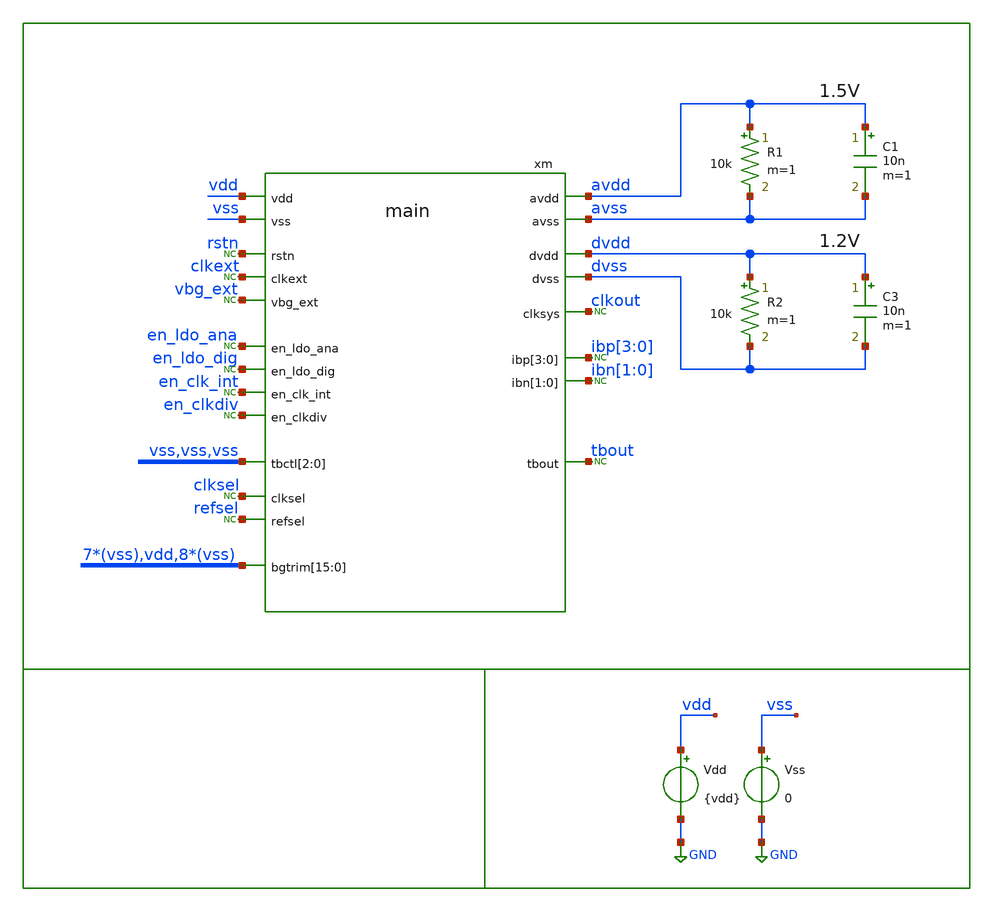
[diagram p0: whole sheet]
** sch_path: xschem/tb/top/tr_main.sch
**.subckt tr_main
Vss vss GND 0
Vdd vdd GND {vdd}
R2 dvdd dvss 10k m=1
* noconn tbout
* noconn rstn
* noconn clkext
* noconn vbg_ext
* noconn en_ldo_ana
* noconn en_ldo_dig
* noconn en_clk_int
* noconn en_clkdiv
* noconn clksel
* noconn refsel
* noconn clkout
C3 dvdd dvss 10n m=1
xm dvdd en_ldo_dig avdd rstn vdd vss en_ldo_ana clkout en_clk_int clkext ibp[3] ibp[2] ibp[1] ibp[0]
+ ibn[1] ibn[0] en_clkdiv clksel refsel vbg_ext avss dvss tbout vss vss vss vss vss vss vss vdd vss vss vss
+ vss vss vss vss vss vss vss vss main
C1 avdd avss 10n m=1
R1 avdd avss 10k m=1
* noconn ibp[3:0]
* noconn ibn[1:0]
**** begin user architecture code
* .include $::SKYWATER_STDCELLS/cells/
.include $::SKYWATER_STDCELLS/cells/buf/sky130_fd_sc_hd__buf_1.spice
.include $::SKYWATER_STDCELLS/cells/clkbuf/sky130_fd_sc_hd__clkbuf_1.spice
.include $::SKYWATER_STDCELLS/cells/clkbuf/sky130_fd_sc_hd__clkbuf_2.spice
.include $::SKYWATER_STDCELLS/cells/clkbuf/sky130_fd_sc_hd__clkbuf_4.spice
.include $::SKYWATER_STDCELLS/cells/clkbuf/sky130_fd_sc_hd__clkbuf_8.spice
.include $::SKYWATER_STDCELLS/cells/clkbuf/sky130_fd_sc_hd__clkbuf_16.spice
.include $::SKYWATER_STDCELLS/cells/decap/sky130_fd_sc_hd__decap_3.spice
.include $::SKYWATER_STDCELLS/cells/decap/sky130_fd_sc_hd__decap_4.spice
.include $::SKYWATER_STDCELLS/cells/decap/sky130_fd_sc_hd__decap_8.spice
.include $::SKYWATER_STDCELLS/cells/dfrbp/sky130_fd_sc_hd__dfrbp_1.spice
.include $::SKYWATER_STDCELLS/cells/dfrbp/sky130_fd_sc_hd__dfrbp_2.spice
.include $::SKYWATER_STDCELLS/cells/inv/sky130_fd_sc_hd__inv_1.spice
.include $::SKYWATER_STDCELLS/cells/inv/sky130_fd_sc_hd__inv_2.spice
.include $::SKYWATER_STDCELLS/cells/inv/sky130_fd_sc_hd__inv_4.spice
.include $::SKYWATER_STDCELLS/cells/mux2/sky130_fd_sc_hd__mux2_2.spice
.include $::SKYWATER_STDCELLS/cells/nand2/sky130_fd_sc_hd__nand2_1.spice
.include $::SKYWATER_STDCELLS/cells/tap/sky130_fd_sc_hd__tap_2.spice
.include $::SKYWATER_STDCELLS/cells/tapvpwrvgnd/sky130_fd_sc_hd__tapvpwrvgnd_1.spice

* Top-level Simulation setup

*-------------------------
* normal setup
*-------------------------
.options method = gear
.options gmin   = 1e-15
.options abstol = 1e-14
.options chtol  = 1e-18
.options reltol = 100e-6
*-------------------------

*-------------------------
* simulator input
*-------------------------
.param MC_SWITCH=0
.param vdd=1.8
.param vss=0

*-------------------------
* includes
*-------------------------
*.include $::DESIGN_PATH/testbuffer/decoder3to8.spice
.include $::DESIGN_PATH/main/main.ext.spice


*-------------------------
* initial conditions
*-------------------------
.ic v(avdd)=0
.ic v(dvdd)=0
.ic v(avss)=0
.ic v(dvss)=0

.ic v(ibp_0_)=0
.ic v(ibp_1_)=0
.ic v(ibp_2_)=0
.ic v(ibp_3_)=0

.ic v(ibn_0_)=0
.ic v(ibn_1_)=0

.ic v(clkout)=0
.ic v(tbout)=0

*-------------------------
* voltage sources
*-------------------------
vrstn rstn vss "dc 0 pulse(1 0 100n 1n 1n 10u 200m)"
vclkext clkext vss 0
vbgext vbg_ext vss 1.2
ven_ldo_ana en_ldo_ana vss {vdd}
ven_ldo_dig en_ldo_dig vss {vdd}
ven_clk_int en_clk_int vss "dc 0 pulse(0 1.8 105u 1n 1n 100m 200m)"
ven_clkdiv en_clkdiv vss 0
vclksel clksel vss 0
vrefsel refsel vss {vdd}

*-------------------------
* simulation
*-------------------------
.tran 100e-9 105e-6 uic
*.tran 100e-9 120e-6 uic
*.tran 10e-9 135e-6 uic

.control
save all
run
echo -------------------
shell date
echo -------------------
.endc
.end


* FET CORNERS
.include $::SKYWATER_MODELS/corners/tt.spice
*.include $::SKYWATER_MODELS/corners/ff.spice
*.include $::SKYWATER_MODELS/corners/ss.spice
*.include $::SKYWATER_MODELS/corners/sf.spice
*.include $::SKYWATER_MODELS/corners/fs.spice

* TT + R + C
*.include $::SKYWATER_MODELS/corners/tt_rmax_cmax.spice
*.include $::SKYWATER_MODELS/corners/tt_rmin_cmin.spice
*.include $::SKYWATER_MODELS/corners/tt_rmax_cmin.spice
*.include $::SKYWATER_MODELS/corners/tt_rmin_cmax.spice

* FF + R + C
*.include $::SKYWATER_MODELS/corners/ff_rmax_cmax.spice
*.include $::SKYWATER_MODELS/corners/ff_rmin_cmin.spice
*.include $::SKYWATER_MODELS/corners/ff_rmax_cmin.spice
*.include $::SKYWATER_MODELS/corners/ff_rmin_cmax.spice


* SS + R + C
*.include $::SKYWATER_MODELS/corners/ss_rmax_cmax.spice
*.include $::SKYWATER_MODELS/corners/ss_rmin_cmin.spice
*.include $::SKYWATER_MODELS/corners/ss_rmax_cmin.spice
*.include $::SKYWATER_MODELS/corners/ss_rmin_cmax.spice

* SF + R + C
*.include $::SKYWATER_MODELS/corners/sf_rmax_cmax.spice
*.include $::SKYWATER_MODELS/corners/sf_rmin_cmin.spice
*.include $::SKYWATER_MODELS/corners/sf_rmax_cmin.spice
*.include $::SKYWATER_MODELS/corners/sf_rmin_cmax.spice

* FS + R + C
*.include $::SKYWATER_MODELS/corners/fs_rmax_cmax.spice
*.include $::SKYWATER_MODELS/corners/fs_rmin_cmin.spice
*.include $::SKYWATER_MODELS/corners/fs_rmax_cmin.spice
*.include $::SKYWATER_MODELS/corners/fs_rmin_cmax.spice

**** end user architecture code
**.ends
.GLOBAL GND
.end
